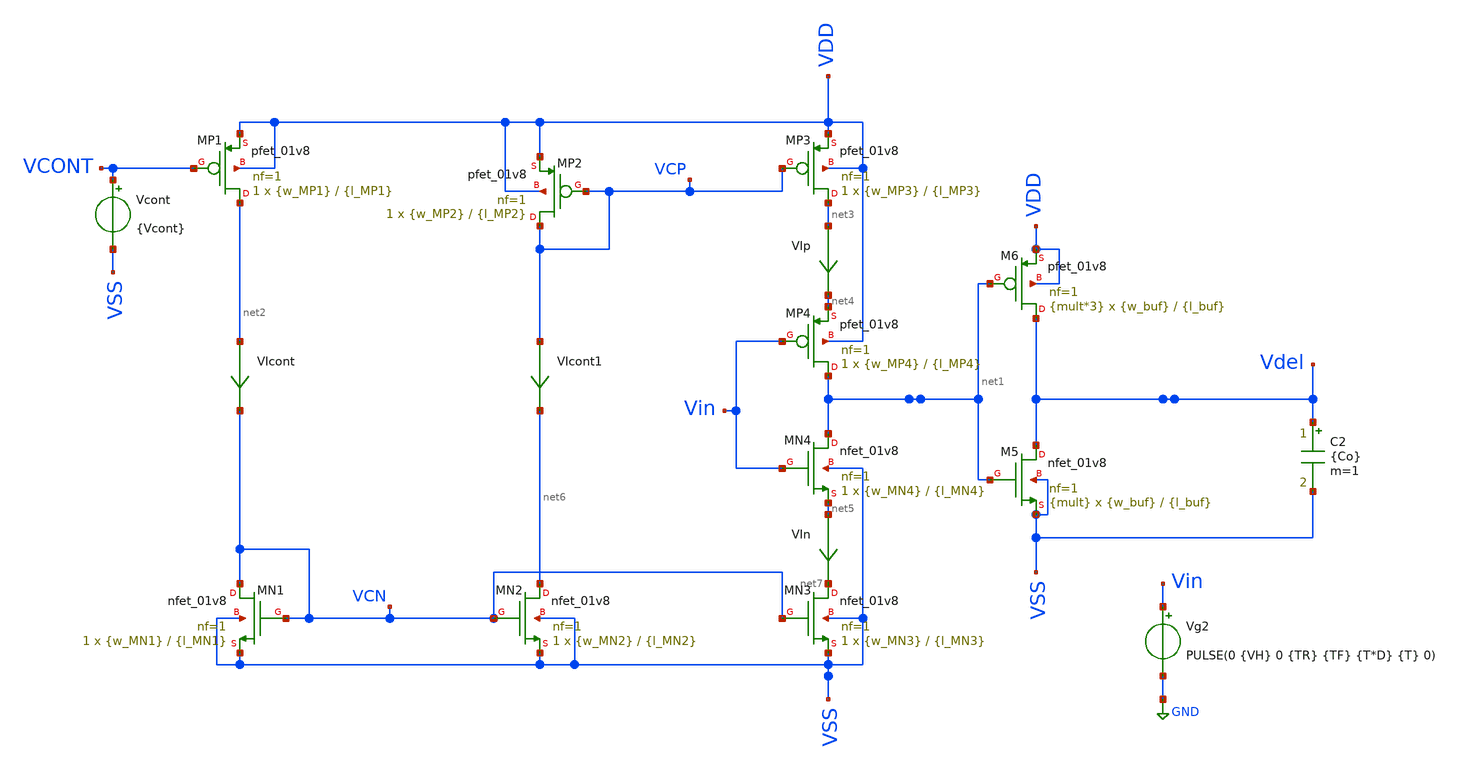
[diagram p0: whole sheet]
** sch_path: xschem/VCO/TB_DelCell_V0_woSymbol.sch
**.subckt TB_DelCell_V0_woSymbol
C2 Vdel VSS {Co} m=1
Vcont VCONT VSS {Vcont}
Vg2 Vin GND PULSE(0 {VH} 0 {TR} {TF} {T*D} {T} 0)
XM5 Vdel net1 VSS VSS sky130_fd_pr__nfet_01v8 L={l_buf} W={w_buf} nf=1 ad='int((nf+1)/2) * W/nf * 0.29'
+ as='int((nf+2)/2) * W/nf * 0.29' pd='2*int((nf+1)/2) * (W/nf + 0.29)' ps='2*int((nf+2)/2) * (W/nf + 0.29)'
+ nrd='0.29 / W' nrs='0.29 / W' sa=0 sb=0 sd=0 mult={mult} m={mult}
XM6 Vdel net1 VDD VDD sky130_fd_pr__pfet_01v8 L={l_buf} W={w_buf} nf=1 ad='int((nf+1)/2) * W/nf * 0.29'
+ as='int((nf+2)/2) * W/nf * 0.29' pd='2*int((nf+1)/2) * (W/nf + 0.29)' ps='2*int((nf+2)/2) * (W/nf + 0.29)'
+ nrd='0.29 / W' nrs='0.29 / W' sa=0 sb=0 sd=0 mult={mult*3} m={mult*3}
XMP1 net2 VCONT VDD VDD sky130_fd_pr__pfet_01v8 L={l_MP1} W={w_MP1} nf=1 ad='int((nf+1)/2) * W/nf * 0.29'
+ as='int((nf+2)/2) * W/nf * 0.29' pd='2*int((nf+1)/2) * (W/nf + 0.29)' ps='2*int((nf+2)/2) * (W/nf + 0.29)'
+ nrd='0.29 / W' nrs='0.29 / W' sa=0 sb=0 sd=0 mult=1 m=1
XMP2 VCP VCP VDD VDD sky130_fd_pr__pfet_01v8 L={l_MP2} W={w_MP2} nf=1 ad='int((nf+1)/2) * W/nf * 0.29'
+ as='int((nf+2)/2) * W/nf * 0.29' pd='2*int((nf+1)/2) * (W/nf + 0.29)' ps='2*int((nf+2)/2) * (W/nf + 0.29)'
+ nrd='0.29 / W' nrs='0.29 / W' sa=0 sb=0 sd=0 mult=1 m=1
XMP3 net3 VCP VDD VDD sky130_fd_pr__pfet_01v8 L={l_MP3} W={w_MP3} nf=1 ad='int((nf+1)/2) * W/nf * 0.29'
+ as='int((nf+2)/2) * W/nf * 0.29' pd='2*int((nf+1)/2) * (W/nf + 0.29)' ps='2*int((nf+2)/2) * (W/nf + 0.29)'
+ nrd='0.29 / W' nrs='0.29 / W' sa=0 sb=0 sd=0 mult=1 m=1
XMP4 net1 Vin net4 VDD sky130_fd_pr__pfet_01v8 L={l_MP4} W={w_MP4} nf=1 ad='int((nf+1)/2) * W/nf * 0.29'
+ as='int((nf+2)/2) * W/nf * 0.29' pd='2*int((nf+1)/2) * (W/nf + 0.29)' ps='2*int((nf+2)/2) * (W/nf + 0.29)'
+ nrd='0.29 / W' nrs='0.29 / W' sa=0 sb=0 sd=0 mult=1 m=1
XMN1 VCN VCN VSS VSS sky130_fd_pr__nfet_01v8 L={l_MN1} W={w_MN1} nf=1 ad='int((nf+1)/2) * W/nf * 0.29'
+ as='int((nf+2)/2) * W/nf * 0.29' pd='2*int((nf+1)/2) * (W/nf + 0.29)' ps='2*int((nf+2)/2) * (W/nf + 0.29)'
+ nrd='0.29 / W' nrs='0.29 / W' sa=0 sb=0 sd=0 mult=1 m=1
XMN2 net6 VCN VSS VSS sky130_fd_pr__nfet_01v8 L={l_MN2} W={w_MN2} nf=1 ad='int((nf+1)/2) * W/nf * 0.29'
+ as='int((nf+2)/2) * W/nf * 0.29' pd='2*int((nf+1)/2) * (W/nf + 0.29)' ps='2*int((nf+2)/2) * (W/nf + 0.29)'
+ nrd='0.29 / W' nrs='0.29 / W' sa=0 sb=0 sd=0 mult=1 m=1
XMN3 net7 VCN VSS VSS sky130_fd_pr__nfet_01v8 L={l_MN3} W={w_MN3} nf=1 ad='int((nf+1)/2) * W/nf * 0.29'
+ as='int((nf+2)/2) * W/nf * 0.29' pd='2*int((nf+1)/2) * (W/nf + 0.29)' ps='2*int((nf+2)/2) * (W/nf + 0.29)'
+ nrd='0.29 / W' nrs='0.29 / W' sa=0 sb=0 sd=0 mult=1 m=1
XMN4 net1 Vin net5 VSS sky130_fd_pr__nfet_01v8 L={l_MN4} W={w_MN4} nf=1 ad='int((nf+1)/2) * W/nf * 0.29'
+ as='int((nf+2)/2) * W/nf * 0.29' pd='2*int((nf+1)/2) * (W/nf + 0.29)' ps='2*int((nf+2)/2) * (W/nf + 0.29)'
+ nrd='0.29 / W' nrs='0.29 / W' sa=0 sb=0 sd=0 mult=1 m=1
VIcont net2 VCN 0
.save i(vicont)
VIp net3 net4 0
.save i(vip)
VIn net5 net7 0
.save i(vin)
VIcont1 VCP net6 0
.save i(vicont1)
**** begin user architecture code

.lib /opt/pdks/sky130A/libs.tech/ngspice/sky130.lib.spice tt
*.lib /opt/pdks/sky130A/libs.tech/ngspice/sky130.lib.spice ss
*.lib /opt/pdks/sky130A/libs.tech/ngspice/sky130.lib.spice ff
*.lib /opt/pdks/sky130A/libs.tech/ngspice/sky130.lib.spice sf
*.lib /opt/pdks/sky130A/libs.tech/ngspice/sky130.lib.spice fs


.param Co = 0.1p
*.param Co = 0.1p
.param mult = 1
.param w_buf = 1
.param l_buf = 0.15

.param Vcont = 0
.param VCP = 0
.param VCN =1.8

vvdd vdd 0 dc 1.8
vvss vss 0 0
*vvcont VCONT 0 dc 0
*vvcont2 VCONT2 0 dc 0
*.option temp = 200
.ic v(V_1) = 0
.ic v(V_2) = 1.8
.save v(V_1) v(Vo)


.param VH = 1.8

.ic v(Vo) = 0

*.param fsw = 10Meg
*.param fsw = 8.4Meg
.param fsw = 1Meg
*.param fsw = 100k

.param T = 1/fsw

.param D = 0.5
.param TR = 1n
.param TF = 1n
.param TdR = 0.5n
.param TdF = 0.5n

.param SimTime =  30*T
.csparam SimTime ={Simtime}
.csparam Tmargin = 10u





.save all
.tran 5n {SimTime}
.csparam start = 10
.control
let Vtarg = 0.9
compose vin_var start=0 stop=0.8 step=0.1

let strt = 0
let stp = 0.8
let step = 0.1
let len2 = 1 + (stp-strt)/step
let Del_sweep = vector(len2)
let DelStarv_sweep = vector(len2)
let index = 0
foreach val $&vin_var
	alter vcont $val
	let f_sum = 0
	let t_act = 0
	let period_cont = 1
	let period_cont2 = 2
	run
	meas tran Tdel TRIG v(Vin) VAL = {Vtarg} RISE = 20 TARG v(Vdel) VAL = {Vtarg}  RISE = 20
	*meas tran TdelStarved TRIG v(Vin) VAL = {Vtarg} RISE = 20 TARG v(Vdel_starved) VAL = {Vtarg}  RISE
+ = 20

	let Del_sweep[index] = Tdel
	let index = index +1
end
plot tran1.v(Vdel)
plot tran8.v(Vdel)

print Del_sweep
plot Del_sweep vs vin_var
.endc




.param w_MP1 = 1
.param l_MP1 = 3
.param w_MP2 = 1
.param l_MP2 = 2
.param w_MP3 = 2
.param l_MP3 = 2
.param w_MP4 = 2
.param l_MP4 = 2

.param w_MN1 = 1
.param l_MN1 = 4
.param w_MN2 = w_MN1
.param l_MN2 = l_MN1
.param w_MN3 = 2
.param l_MN3 = 4
.param w_MN4 = 2
.param l_MN4 = 4



**** end user architecture code
**.ends
.GLOBAL GND
.end
